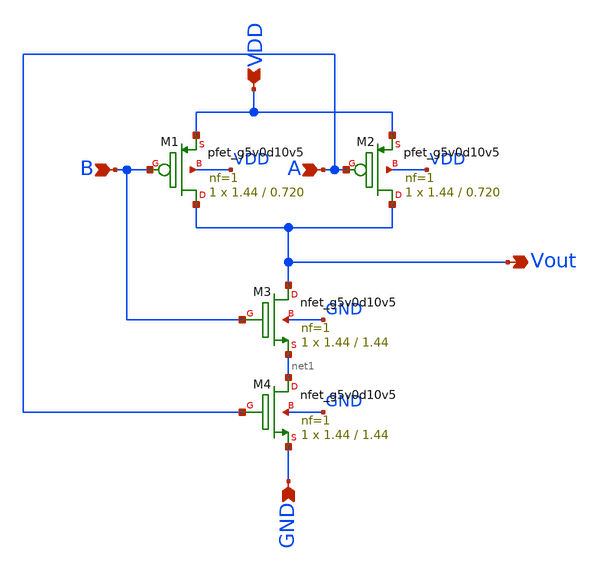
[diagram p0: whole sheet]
** sch_path: xschem/Nand_Gate.sch
**.subckt Nand_Gate A B VDD GND Vout
*.ipin A
*.ipin B
*.ipin VDD
*.ipin GND
*.opin Vout
XM1 Vout B VDD VDD sky130_fd_pr__pfet_g5v0d10v5 L=0.720 W=1.44 nf=1 ad='int((1 + 1)/2) * 1.44 / 1 * 0.29'
+ as='int((1 + 2)/2) * 1.44 / 1 * 0.29' pd='2*int((1 + 1)/2) * (1.44 / 1 + 0.29)' ps='2*int((1 + 2)/2) * (1.44 / 1 + 0.29)'
+ nrd='0.29 / 1.44 ' nrs='0.29 / 1.44 ' sa=0 sb=0 sd=0 mult=1 m=1
XM2 Vout A VDD VDD sky130_fd_pr__pfet_g5v0d10v5 L=0.720 W=1.44 nf=1 ad='int((1 + 1)/2) * 1.44 / 1 * 0.29'
+ as='int((1 + 2)/2) * 1.44 / 1 * 0.29' pd='2*int((1 + 1)/2) * (1.44 / 1 + 0.29)' ps='2*int((1 + 2)/2) * (1.44 / 1 + 0.29)'
+ nrd='0.29 / 1.44 ' nrs='0.29 / 1.44 ' sa=0 sb=0 sd=0 mult=1 m=1
XM3 Vout B net1 GND sky130_fd_pr__nfet_g5v0d10v5 L=1.44 W=1.44 nf=1 ad='int((1 + 1)/2) * 1.44 / 1 * 0.29'
+ as='int((1 + 2)/2) * 1.44 / 1 * 0.29' pd='2*int((1 + 1)/2) * (1.44 / 1 + 0.29)' ps='2*int((1 + 2)/2) * (1.44 / 1 + 0.29)'
+ nrd='0.29 / 1.44 ' nrs='0.29 / 1.44 ' sa=0 sb=0 sd=0 mult=1 m=1
XM4 net1 A GND GND sky130_fd_pr__nfet_g5v0d10v5 L=1.44 W=1.44 nf=1 ad='int((1 + 1)/2) * 1.44 / 1 * 0.29'
+ as='int((1 + 2)/2) * 1.44 / 1 * 0.29' pd='2*int((1 + 1)/2) * (1.44 / 1 + 0.29)' ps='2*int((1 + 2)/2) * (1.44 / 1 + 0.29)'
+ nrd='0.29 / 1.44 ' nrs='0.29 / 1.44 ' sa=0 sb=0 sd=0 mult=1 m=1
**.ends
.end
